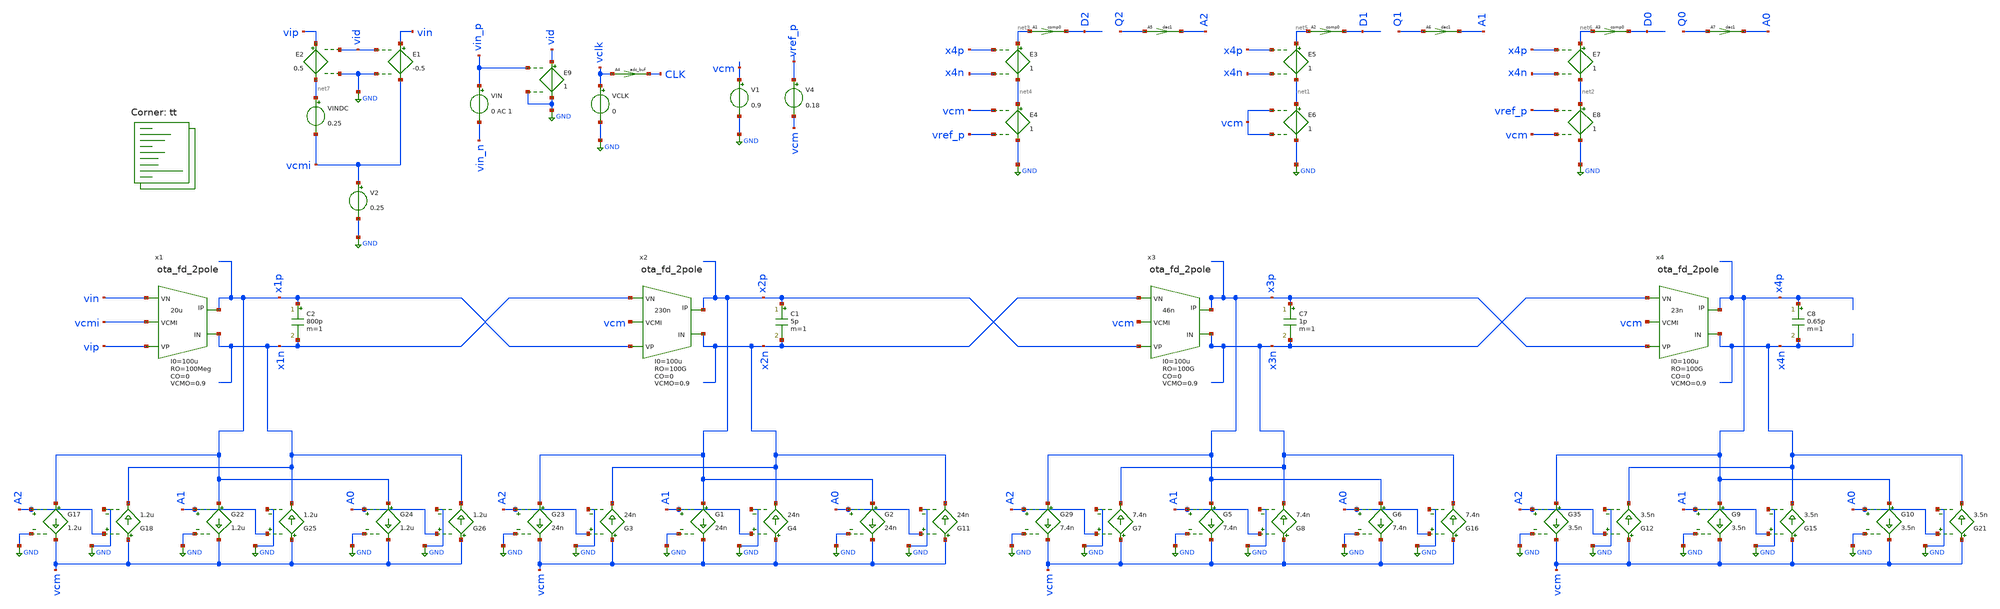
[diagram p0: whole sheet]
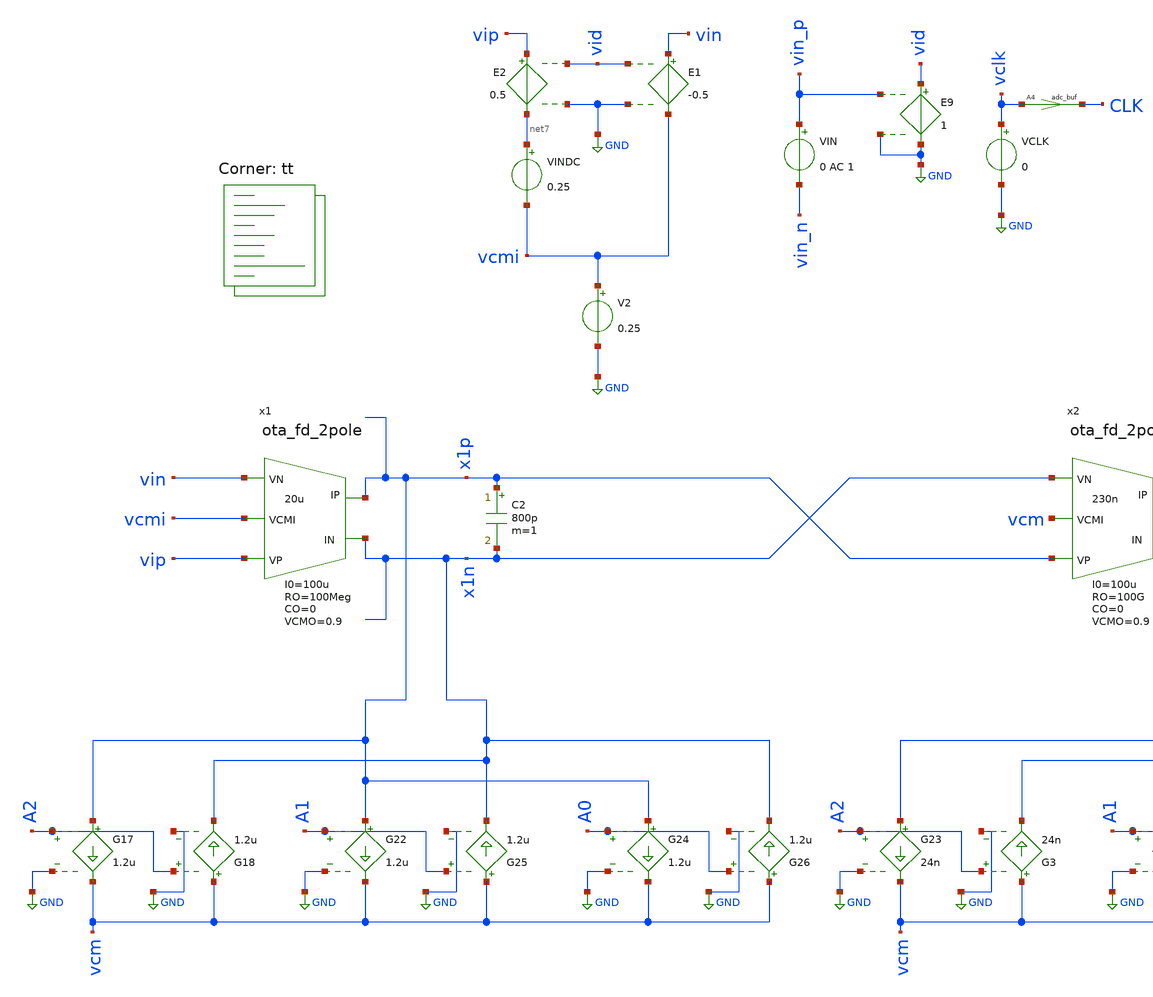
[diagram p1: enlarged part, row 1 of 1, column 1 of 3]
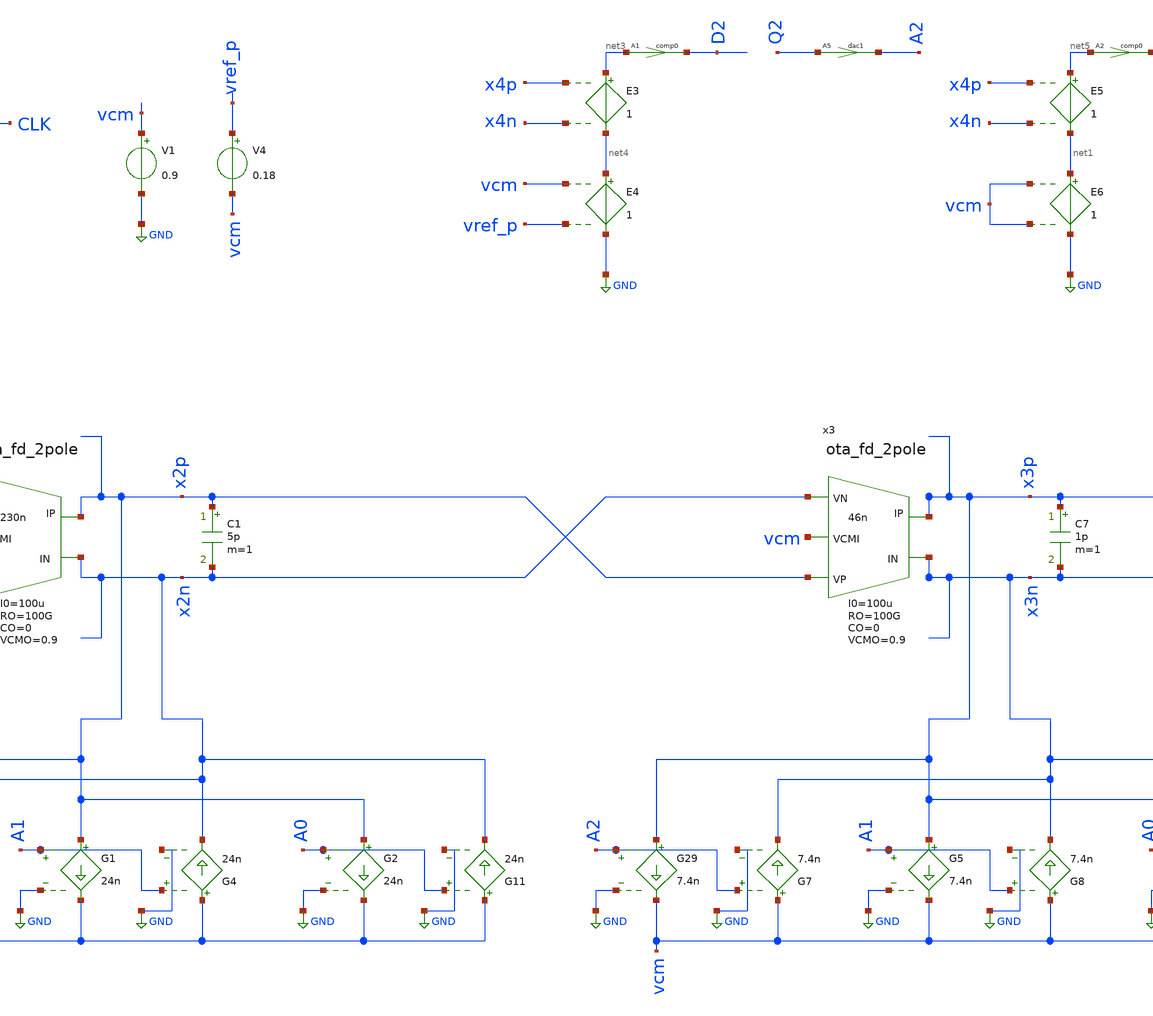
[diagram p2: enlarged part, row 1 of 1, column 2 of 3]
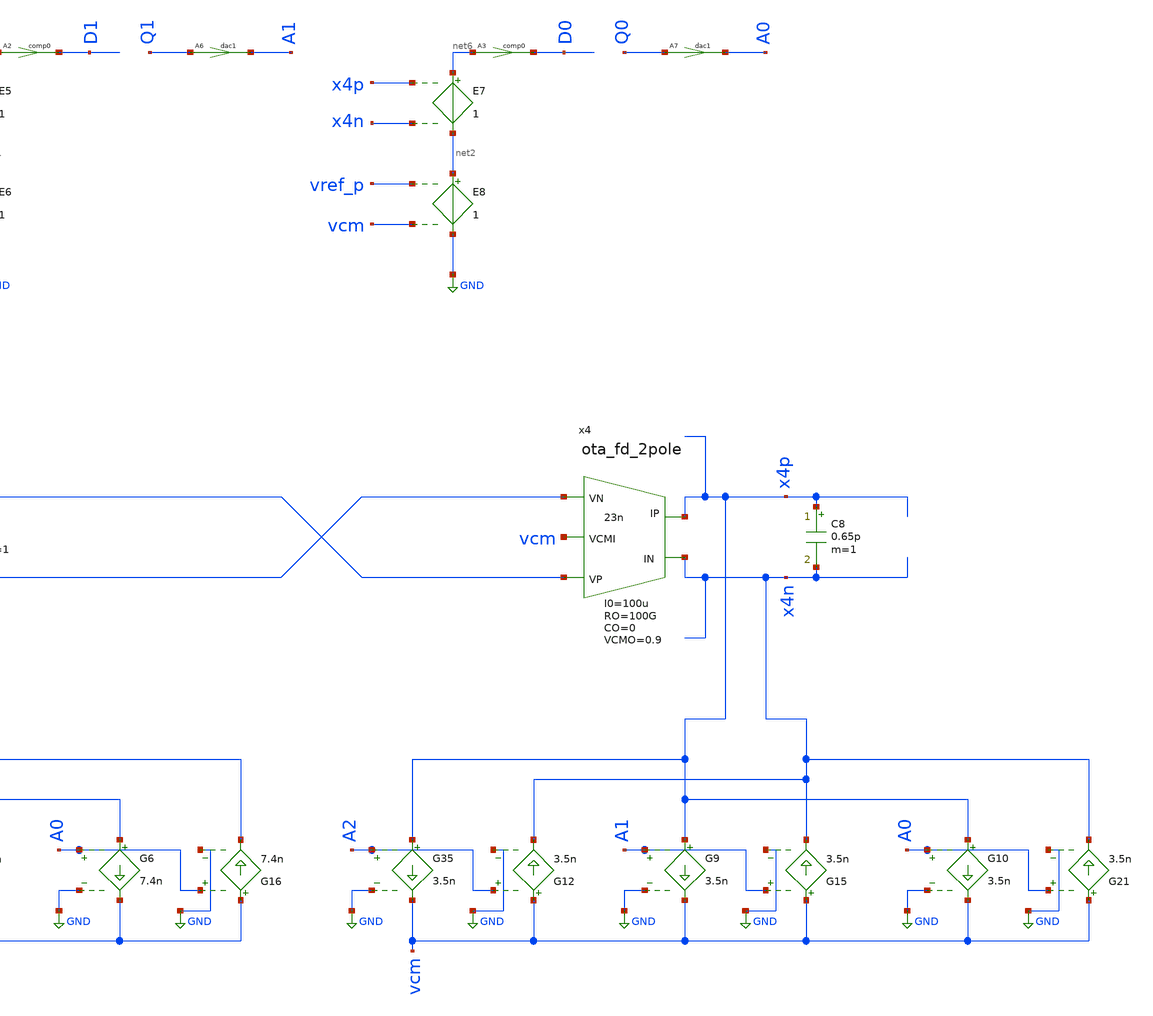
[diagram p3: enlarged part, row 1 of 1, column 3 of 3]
** sch_path: circuit-level/xschem/dsm/ctmod4_2bit_fb.sch
**.subckt ctmod4_2bit_fb
V2 vcmi GND 0.25
E1 vin vcmi vid GND -0.5
E2 vip net7 vid GND 0.5
VIN vin_p vin_n 0 AC 1
V1 vcm GND 0.9
A1 [ net3 ] [ D2 ] comp0
E3 net3 net4 x4p x4n 1
E4 net4 GND vcm vref_p 1
A2 [ net5 ] [ D1 ] comp0
E5 net5 net1 x4p x4n 1
E6 net1 GND vcm vcm 1
A3 [ net6 ] [ D0 ] comp0
E7 net6 net2 x4p x4n 1
E8 net2 GND vref_p vcm 1
A5 [ Q2 ] [ A2 ] dac1
A6 [ Q1 ] [ A1 ] dac1
A7 [ Q0 ] [ A0 ] dac1
G17 x1p vcm A2 GND 1.2u
G18 vcm x1n A2 GND 1.2u
G22 x1p vcm A1 GND 1.2u
G24 x1p vcm A0 GND 1.2u
VCLK vclk GND 0
A4 [ vclk ] [ CLK ] adc_buf
V4 vref_p vcm 0.18
VINDC net7 vcmi 0.25
G23 x2p vcm A2 GND 24n
G1 x2p vcm A1 GND 24n
G2 x2p vcm A0 GND 24n
G29 x3p vcm A2 GND 7.4n
G5 x3p vcm A1 GND 7.4n
G6 x3p vcm A0 GND 7.4n
G35 x4p vcm A2 GND 3.5n
G9 x4p vcm A1 GND 3.5n
G10 x4p vcm A0 GND 3.5n
C2 x1p x1n 800p m=1
x1 vin x1p x1n vip vcmi ota_fd_2pole GM=20u RO=100Meg CO=0 RP=0 CP=0 VCMO=0.9 I0=100u
C1 x2p x2n 5p m=1
x2 x1n x2p x2n x1p vcm ota_fd_2pole GM=230n RO=100G CO=0 RP=0 CP=0 VCMO=0.9 I0=100u
C7 x3p x3n 1p m=1
x3 x2n x3p x3n x2p vcm ota_fd_2pole GM=46n RO=100G CO=0 RP=0 CP=0 VCMO=0.9 I0=100u
C8 x4p x4n 0.65p m=1
x4 x3n x4p x4n x3p vcm ota_fd_2pole GM=23n RO=100G CO=0 RP=0 CP=0 VCMO=0.9 I0=100u
E9 vid GND vin_p GND 1
G25 vcm x1n A1 GND 1.2u
G26 vcm x1n A0 GND 1.2u
G3 vcm x2n A2 GND 24n
G4 vcm x2n A1 GND 24n
G11 vcm x2n A0 GND 24n
G7 vcm x3n A2 GND 7.4n
G8 vcm x3n A1 GND 7.4n
G16 vcm x3n A0 GND 7.4n
G12 vcm x4n A2 GND 3.5n
G15 vcm x4n A1 GND 3.5n
G21 vcm x4n A0 GND 3.5n
**** begin user architecture code
.lib $::SKYWATER_MODELS/sky130.lib.spice tt


** XSPICE Component Instances
a24 D0 CLK NULL NULL %d(Q0 NQ0) dff1
a25 D1 CLK NULL NULL %d(Q1 NQ1) dff1
a26 D2 CLK NULL NULL %d(Q2 NQ2) dff1
a27 NQ1 %d(B1) inv1
a28 [NQ1 Q0] temp1 and1
a29 [Q2 temp1] %d(B0) or1

** XSPICE Models
.model comp0 adc_bridge(in_low=-1e-15 in_high=0)
.model adc_buf adc_bridge(in_low=0.899 in_high=0.901)
.model dac1 dac_bridge(out_low = -1 out_high = 1 out_undef = -1 input_load = 5.0e-12 t_rise = 0.1e-9
+ t_fall = 0.1e-9)
.model dac2 dac_bridge(out_low = 0 out_high = 1 out_undef = -1 input_load = 0 t_rise = 0.50e-9
+ t_fall = 0.50e-9)
.model switch1 sw vt=0.9 vh=0.05 ron=0.1 roff=100Meg
.model inv1 d_inverter(rise_delay = 0.5e-9 fall_delay = 0.5e-9 input_load = 0.5e-12)
.model and1 d_and(rise_delay = 0.5e-9 fall_delay = 0.3e-9 input_load = 0.5e-12)
.model or1 d_or(rise_delay = 0.5e-9 fall_delay = 0.3e-9 input_load = 0.5e-12)
.model dff1 d_dff(clk_delay = 10.0e-9 set_delay = 10.0e-9 reset_delay = 10.0e-9 ic = 0 rise_delay =
+ 10.0e-9 fall_delay = 10.0e-9)

** Transient Noise Source
VNoiw vin_n 0 DC 0 TRNOISE (0 1.5u 0 0)

** Save specific nodes
*.options savecurrents
.control
esave CLK B1 B0
*save vclk x1p x1n x2p x2n x3p x3n x4p x4n vip vin data1 data0 A0 A1 A2
*save x1p x1n x2p x2n x3p x3n x4p x4n vip vin

set notrnoise

let tstartup = 0

let f_res = 1/64
let f_sig = 18
let tper_sig = 1/f_sig
let tfr_sig = tper_sig/2

let vin_ampl = 0.01
let vin_dc = 0.25

alter @VIN[SIN] = [ 0 $&vin_ampl $&f_sig $&tstartup 0 0 ]
alter @VIN[DC] = 0.0
alter @VINDC[DC] = $&vin_dc

let fs = 65536
let fclk = fs
let tper_clk = 1/fclk
let tfr_clk = tper_clk/100
let ton_clk = tper_clk*5/10
alter @VCLK[PULSE]=[ 0 1.8 $&tstartup $&tfr_clk $&tfr_clk $&ton_clk $&tper_clk 0 ]

let N_per = f_sig/f_res
let N_per = 2
let tstep = 0.01/f_sig
let tstop = N_per/f_sig
let tstart = 0

** Main Simulations
let pltnr = 1

while const.pltnr le 1

	*dc VIN -0.81 0.81 0.008

	*ac dec 1000 0.1 1e7

	tran $&tstep $&tstop $&tstart uic


	*set pltName = ac$&const.pltnr
       	*setplot $pltName
	*setplot ac1
	*let A = v(vout)/v(vin)
	*plot vdb(A) 180/PI*cph(A)

	*set pltName = dc$&const.pltnr
       	*setplot $pltName
	*setplot dc1
	*let vid = v(vid)


	*let iop = v1#branch
	*let ion = v3#branch
	*let iod = iop-ion

	*plot iod ion iop

	setplot tran1

	eprvcd CLK B0 B1 > /foss/designs/mod/ctdsm4_tran_out.vcd

	*let x1d = v(x1p)-v(x1n)
	*let x2d = v(x2p)-v(x2n)
	*let x3d = v(x3p)-v(x3n)
	*let x4d = v(x4p)-v(x4n)
	*let vin = v(vip)-v(vin)

	*let x1cm = (v(x1p)+v(x1n))/2
	*let x2cm = (v(x2p)+v(x2n))/2
	*let x3cm = (v(x3p)+v(x3n))/2
	*let x4cm = (v(x4p)+v(x4n))/2

	*let i1op = vx1p#branch
	*let i1on = vx1n#branch
	*let i2op = vx2p#branch
	*let i2on = vx2n#branch
	*let i3op = vx3p#branch
	*let i3on = vx3n#branch
	*let i4op = vx4p#branch
	*let i4on = vx4n#branch

	*let i1fbp = vfb1p#branch
	*let i1fbn = vfb1n#branch
	*let i2fbp = vfb2p#branch
	*let i2fbn = vfb2n#branch
	*let i3fbp = vfb3p#branch
	*let i3fbn = vfb3n#branch
	*let i4fbp = vfb4p#branch
	*let i4fbn = vfb4n#branch

	*let i1o = i1op - i1on
	*let i1fb = i1fbp - i1fbn
	*let i2o = i2op - i2on
	*let i2fb = i2fbp - i2fbn
	*let i3o = i3op - i3on
	*let i3fb = i3fbp - i3fbn
	*let i4o = i4op - i4on
	*let i4fb = i4fbp - i4fbn

	*plot vin x1d x2d x3d x4d
	*plot x1cm x2cm x3cm x4cm
	*plot A0 A1 A2
	*plot i1op i1on i1fbp i1fbn
	*plot i2op i2on i2fbp i2fbn
	*plot i3op i3on i3fbp i3fbn
	*plot i4op i4on i4fbp i4fbn
	*plot i1o i1fb
	*plot i2o i2fb
	*plot i3o i3fb
	*plot i4o i4fb
	*plot i2op i2on
	*plot i3op i3on
	*plot i4op i4on

	*plot vin


       	let const.pltnr = const.pltnr + 1
end

.endc

**** end user architecture code
**.ends

* expanding   symbol:  /foss/designs/macro-models/ota_fd_2pole.sym # of pins=5
** sym_path: circuit-level/xschem/macro-models/ota_fd_2pole.sym
** sch_path: circuit-level/xschem/macro-models/ota_fd_2pole.sch
.subckt ota_fd_2pole VN IP IN VP VCMI  GM=1u RO=100Meg CO=1p RP=0 CP=0.1p VCMO=0 I0=1u
*.ipin VP
*.ipin VN
*.opin IP
*.opin IN
*.ipin VCMI
R3 IP net1 {{RO}/2} m=1
R4 IN net1 {{RO}/2} m=1
C3 IP net1 {2*{CO}} m=1
R5 VN ip1 {RP} m=1
C4 ip1 VCMI {CP} m=1
C6 in1 VCMI {CP} m=1
C8 IN net1 {2*{CO}} m=1
R7 VP in1 {RP} m=1
B2 IP net1 I = {{I0}*tanh({GM}/2*V(ip1,in1)/{I0})}
B1 net1 IN I = {{I0}*tanh({GM}/2*V(ip1,in1)/{I0})}
B5 net1 GND I = {{VCMO}-(V(IP)+V(IN))/2}
.ends

.GLOBAL GND
.end
